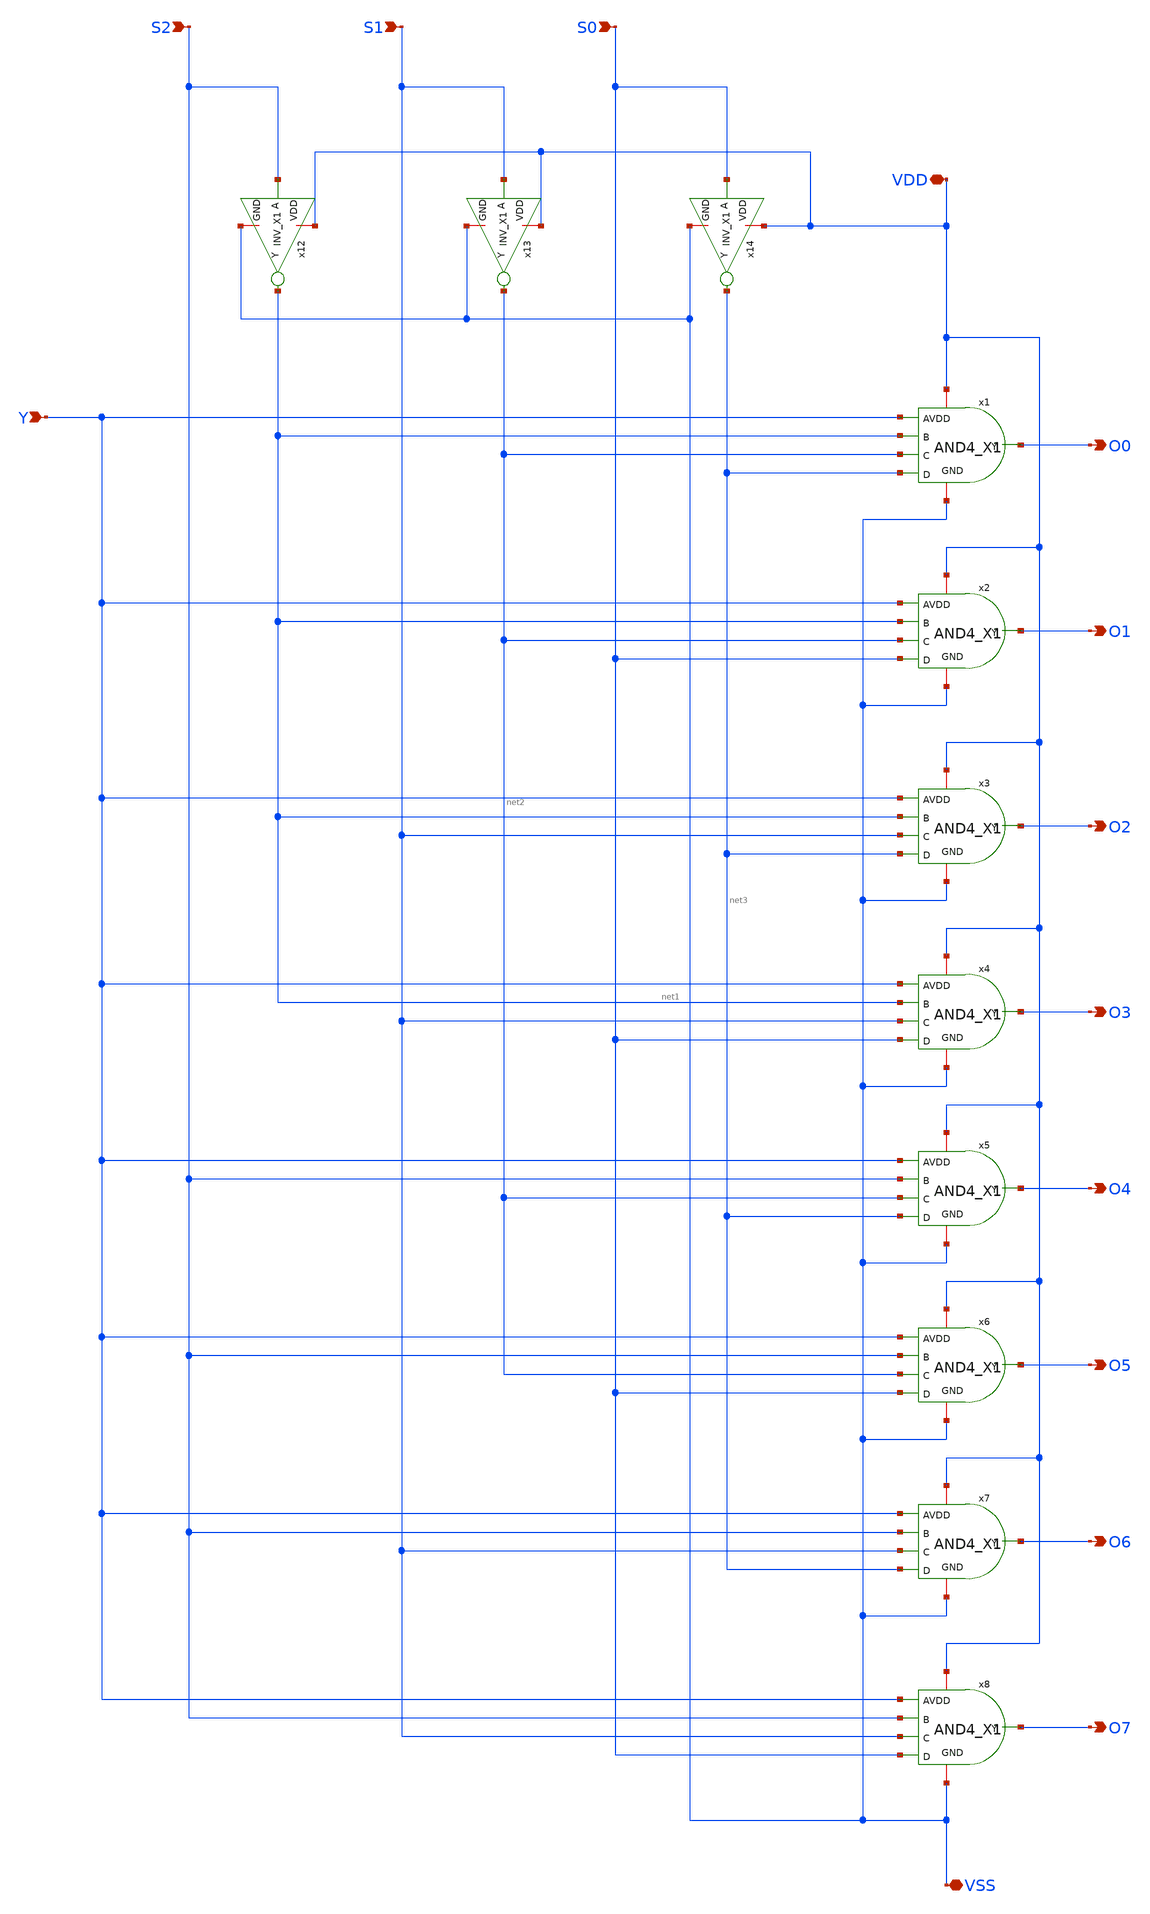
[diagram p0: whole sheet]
** sch_path: schematic/20250924_OSS_Workshop/Qdai/inverter_MUX_01/DEMUX8.sch
**.subckt DEMUX8 VDD VSS S2 S1 S0 O7 Y O6 O5 O4 O3 O2 O1 O0
*.iopin VDD
*.iopin VSS
*.ipin S2
*.ipin S1
*.ipin S0
*.opin O7
*.ipin Y
*.opin O6
*.opin O5
*.opin O4
*.opin O3
*.opin O2
*.opin O1
*.opin O0
x1 net3 net2 VDD O0 Y net1 VSS AND4_X1
x2 S0 net2 VDD O1 Y net1 VSS AND4_X1
x3 net3 S1 VDD O2 Y net1 VSS AND4_X1
x4 S0 S1 VDD O3 Y net1 VSS AND4_X1
x5 net3 net2 VDD O4 Y S2 VSS AND4_X1
x6 S0 net2 VDD O5 Y S2 VSS AND4_X1
x7 net3 S1 VDD O6 Y S2 VSS AND4_X1
x8 S0 S1 VDD O7 Y S2 VSS AND4_X1
x12 VDD S2 net1 VSS INV_X1
x13 VDD S1 net2 VSS INV_X1
x14 VDD S0 net3 VSS INV_X1
**.ends

* expanding   symbol:  IP62_5_stdcell/AND4_X1.sym # of pins=7
** sym_path: openIP62_rev1.0/IP62/Technology/tech/symbols/Xschem/IP62_5_stdcell/AND4_X1.sym
** sch_path: openIP62_rev1.0/IP62/Technology/tech/symbols/Xschem/IP62_5_stdcell/AND4_X1.sch
.subckt AND4_X1 D C VDD Y A B GND
*.opin Y
*.ipin A
*.ipin B
*.iopin VDD
*.iopin GND
*.ipin C
*.ipin D
XM7 net1 A net4 GND NMOS w=3.4u l=1u as=0 ad=0 ps=0 pd=0 nrd=0 nrs=0 m=1
XM5 net3 C net2 GND NMOS w=3.4u l=1u as=0 ad=0 ps=0 pd=0 nrd=0 nrs=0 m=1
XM8 Y net1 GND GND NMOS w=3.4u l=1u as=0 ad=0 ps=0 pd=0 nrd=0 nrs=0 m=1
XM10 net2 D GND GND NMOS w=3.4u l=1u as=0 ad=0 ps=0 pd=0 nrd=0 nrs=0 m=1
XM6 net4 B net3 GND NMOS w=3.4u l=1u as=0 ad=0 ps=0 pd=0 nrd=0 nrs=0 m=1
XM11 net1 A VDD VDD PMOS w=10.2u l=1u as=0 ad=0 ps=0 pd=0 nrd=0 nrs=0 m=1
XM1 net1 D VDD VDD PMOS w=10.2u l=1u as=0 ad=0 ps=0 pd=0 nrd=0 nrs=0 m=1
XM3 net1 C VDD VDD PMOS w=10.2u l=1u as=0 ad=0 ps=0 pd=0 nrd=0 nrs=0 m=1
XM4 Y net1 VDD VDD PMOS w=10.2u l=1u as=0 ad=0 ps=0 pd=0 nrd=0 nrs=0 m=1
XM2 net1 B VDD VDD PMOS w=10.2u l=1u as=0 ad=0 ps=0 pd=0 nrd=0 nrs=0 m=1
.ends


* expanding   symbol:  IP62_5_stdcell/INV_X1.sym # of pins=4
** sym_path: openIP62_rev1.0/IP62/Technology/tech/symbols/Xschem/IP62_5_stdcell/INV_X1.sym
** sch_path: openIP62_rev1.0/IP62/Technology/tech/symbols/Xschem/IP62_5_stdcell/INV_X1.sch
.subckt INV_X1 VDD A Y GND
*.ipin A
*.opin Y
*.iopin GND
*.iopin VDD
XM7 Y A VDD VDD PMOS w=10.2u l=1u as=0 ad=0 ps=0 pd=0 nrd=0 nrs=0 m=1
XM2 Y A GND GND NMOS w=3.4u l=1u as=0 ad=0 ps=0 pd=0 nrd=0 nrs=0 m=1
.ends

.end
